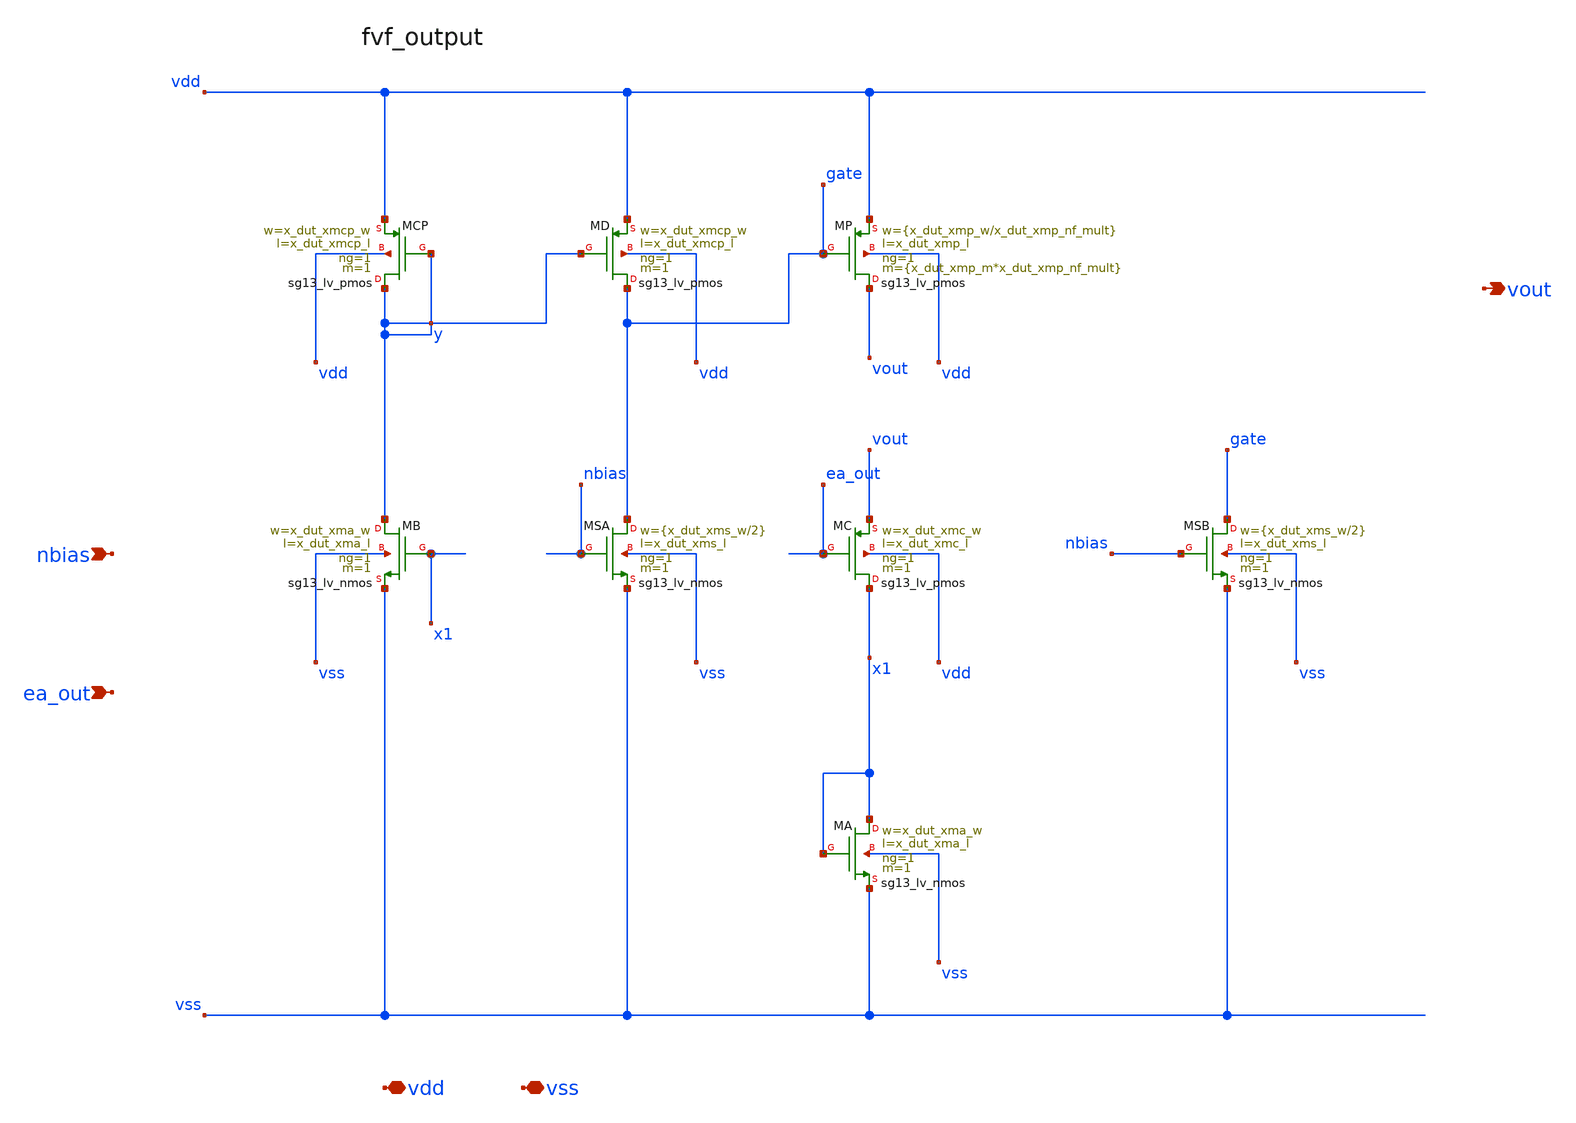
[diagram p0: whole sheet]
** sch_path: analog-db/circuits/ldo_010_capless_lowiq/pdk/ihp-sg13g2/schematic/blocks/fvf_output.sch
**.subckt fvf_output nbias ea_out vdd vss vout
*.ipin nbias
*.ipin ea_out
*.iopin vdd
*.iopin vss
*.opin vout
XMC x1 ea_out vout vdd sg13_lv_pmos w=x_dut_xmc_w l=x_dut_xmc_l ng=1 m=1 mm_ok=1
XMA x1 x1 vss vss sg13_lv_nmos w=x_dut_xma_w l=x_dut_xma_l ng=1 m=1 mm_ok=1
XMB y x1 vss vss sg13_lv_nmos w=x_dut_xma_w l=x_dut_xma_l ng=1 m=1 mm_ok=1
XMCP y y vdd vdd sg13_lv_pmos w=x_dut_xmcp_w l=x_dut_xmcp_l ng=1 m=1 mm_ok=1
XMD gate y vdd vdd sg13_lv_pmos w=x_dut_xmcp_w l=x_dut_xmcp_l ng=1 m=1 mm_ok=1
XMSA gate nbias vss vss sg13_lv_nmos w={x_dut_xms_w/2} l=x_dut_xms_l ng=1 m=1 mm_ok=1
XMSB gate nbias vss vss sg13_lv_nmos w={x_dut_xms_w/2} l=x_dut_xms_l ng=1 m=1 mm_ok=1
XMP vout gate vdd vdd sg13_lv_pmos w={x_dut_xmp_w/x_dut_xmp_nf_mult} l=x_dut_xmp_l ng=1 m={x_dut_xmp_m*x_dut_xmp_nf_mult}
+ mm_ok=1
**.ends
.end
